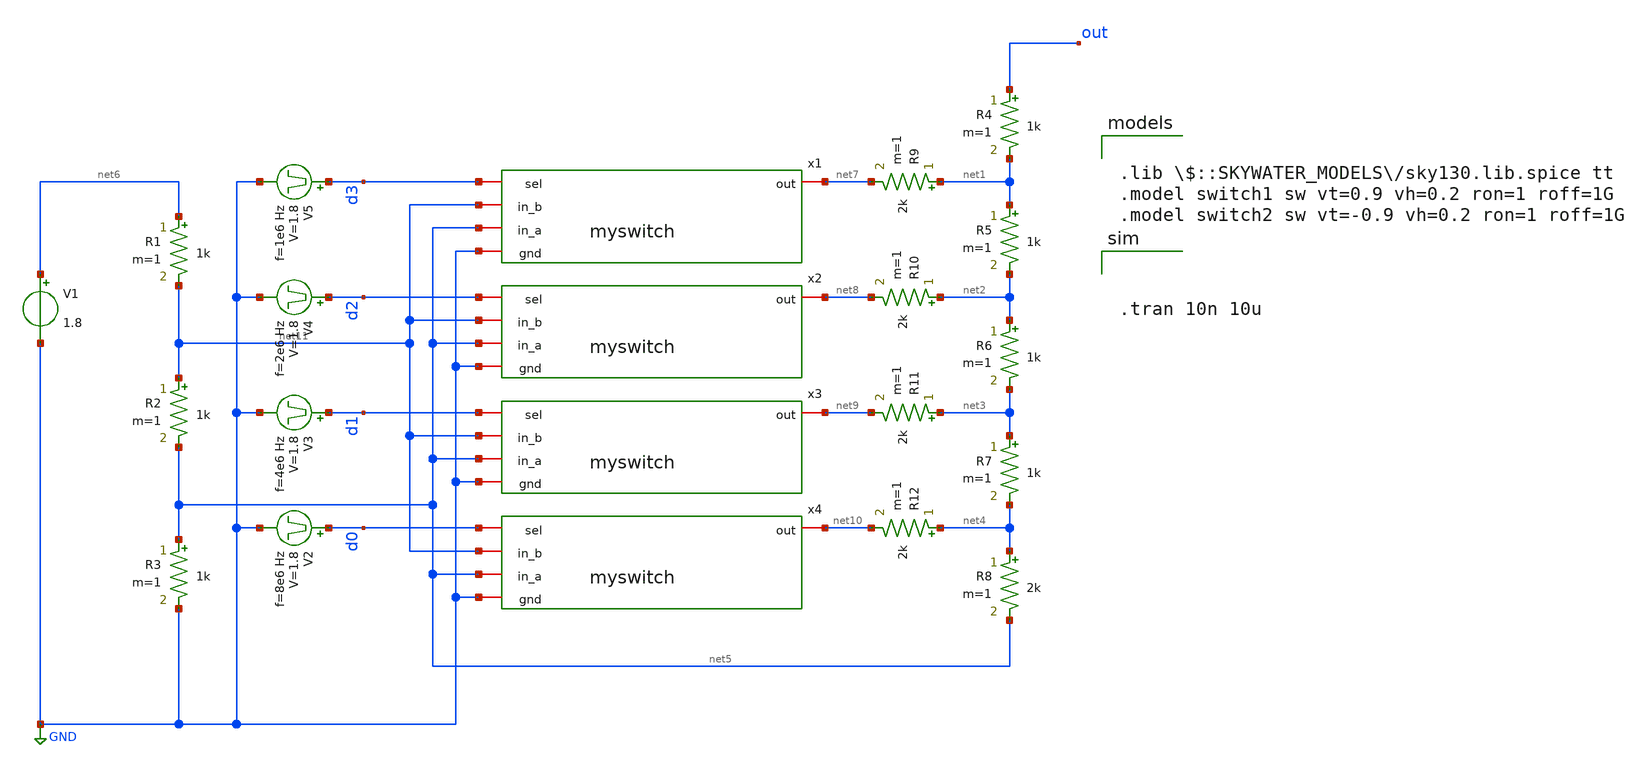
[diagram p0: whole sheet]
** sch_path: design/myopamp/test/r-2r_tb.sch
**.subckt r-2r_tb
R4 out net1 1k m=1
R5 net1 net2 1k m=1
R6 net2 net3 1k m=1
R7 net3 net4 1k m=1
R8 net4 net5 2k m=1
R9 net1 net7 2k m=1
R10 net2 net8 2k m=1
R11 net3 net9 2k m=1
R12 net4 net10 2k m=1
V1 net6 GND 1.8
R1 net6 net11 1k m=1
R2 net11 net5 1k m=1
R3 net5 GND 1k m=1
x1 net7 d3 GND net11 net5 myswitch
x2 net8 d2 GND net11 net5 myswitch
x3 net9 d1 GND net11 net5 myswitch
x4 net10 d0 GND net11 net5 myswitch
V2 d0 GND pulse 0 1.8 '0.495/ 8e6 ' '0.01/8e6 ' '0.01/8e6 ' '0.49/8e6 ' '1/8e6 '
V3 d1 GND pulse 0 1.8 '0.495/ 4e6 ' '0.01/4e6 ' '0.01/4e6 ' '0.49/4e6 ' '1/4e6 '
V4 d2 GND pulse 0 1.8 '0.495/ 2e6 ' '0.01/2e6 ' '0.01/2e6 ' '0.49/2e6 ' '1/2e6 '
V5 d3 GND pulse 0 1.8 '0.495/ 1e6 ' '0.01/1e6 ' '0.01/1e6 ' '0.49/1e6 ' '1/1e6 '
**** begin user architecture code



.tran 10n 10u



.lib $::SKYWATER_MODELS/sky130.lib.spice tt
.model switch1 sw vt=0.9 vh=0.2 ron=1 roff=1G
.model switch2 sw vt=-0.9 vh=0.2 ron=1 roff=1G


**** end user architecture code
**.ends

* expanding   symbol:  myopamp/myswitch.sym # of pins=5
** sym_path: design/myopamp/myswitch.sym
** sch_path: design/myopamp/myswitch.sch
.subckt myswitch out sel gnd in_b in_a
*.iopin gnd
*.iopin sel
*.iopin out
*.iopin in_a
*.iopin in_b
S1 out in_b sel gnd SWITCH1
S2 out in_a gnd sel SWITCH2
.ends

.GLOBAL GND
.end
